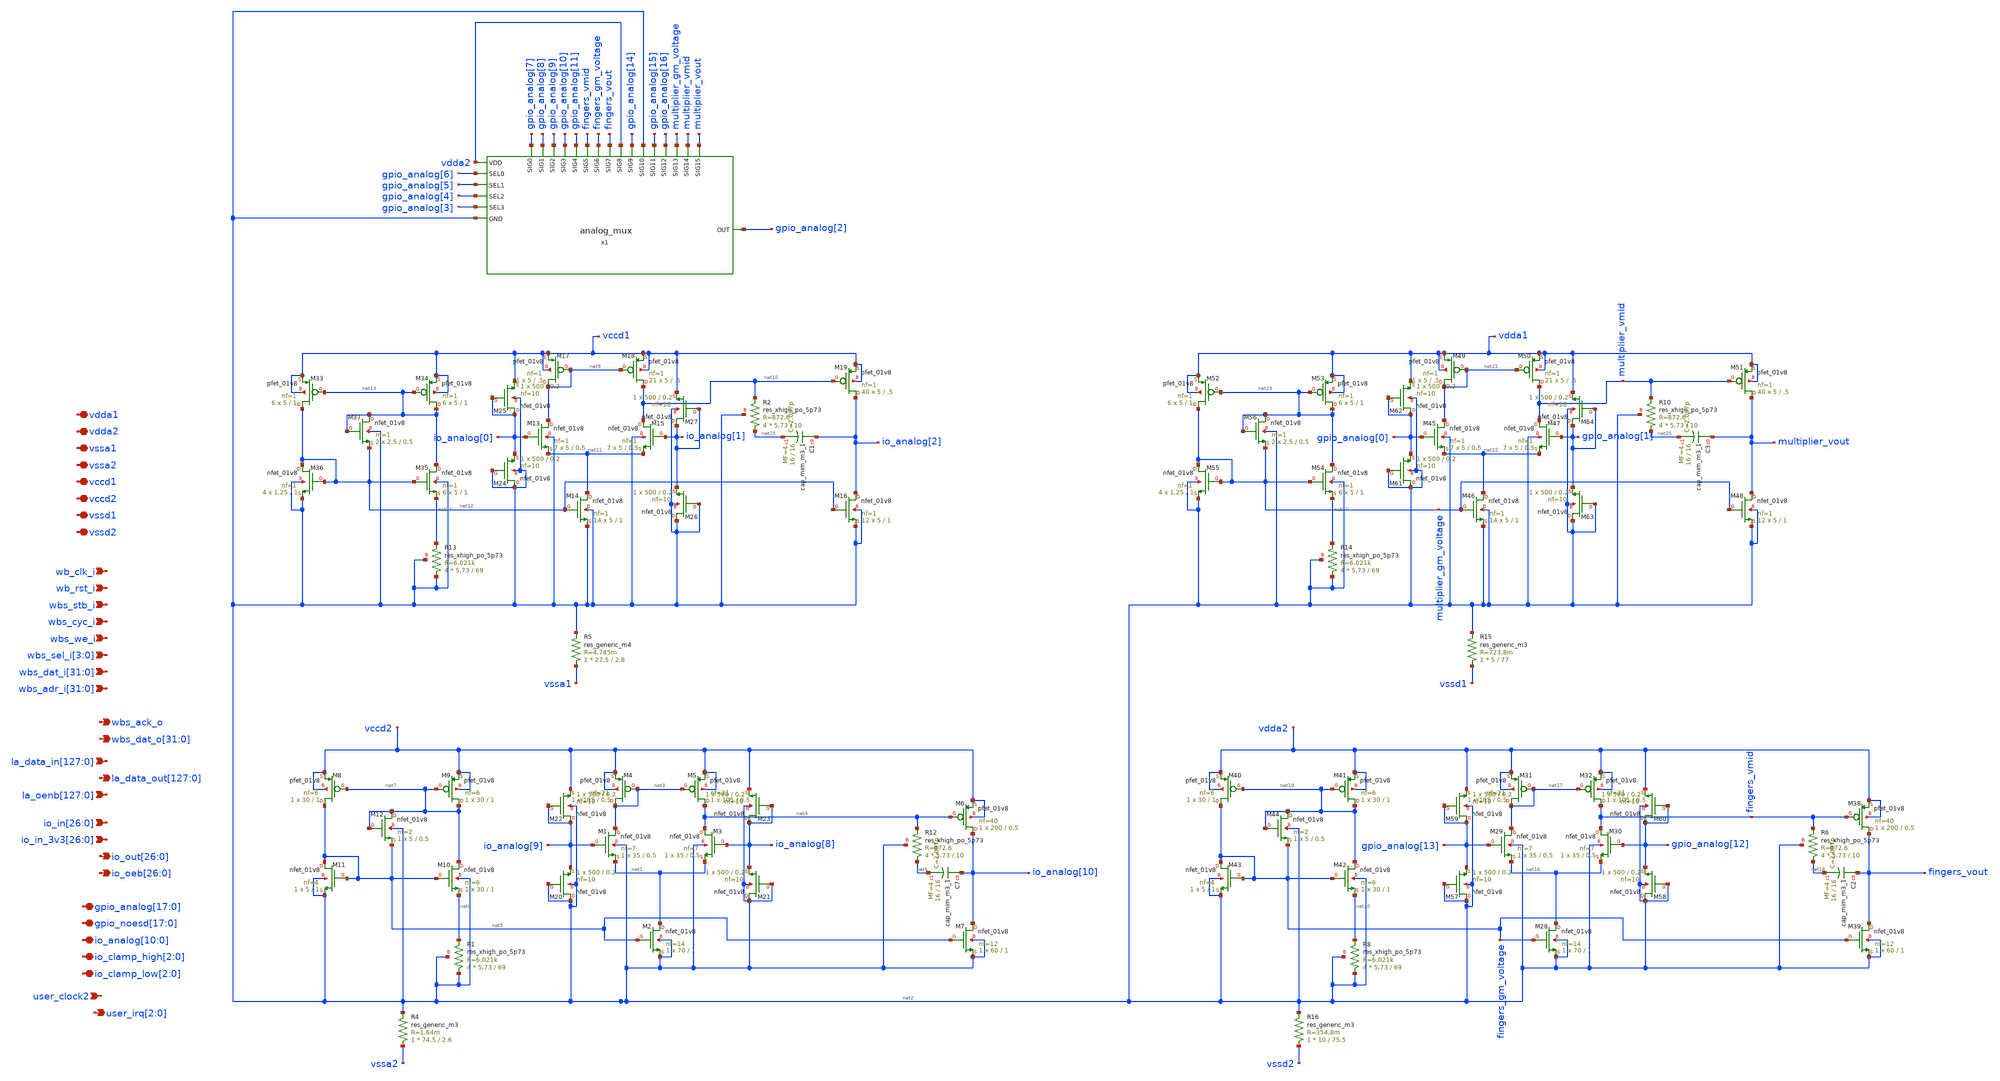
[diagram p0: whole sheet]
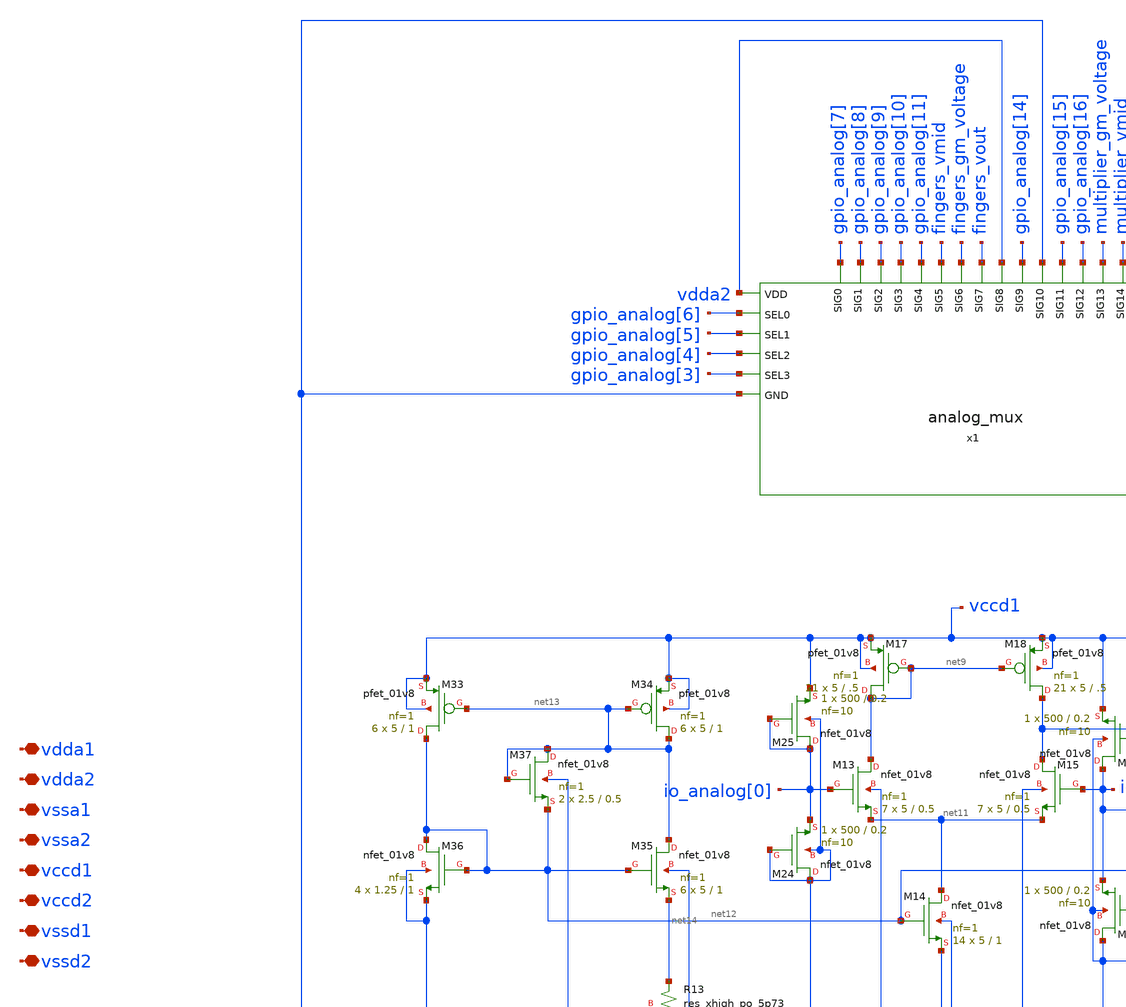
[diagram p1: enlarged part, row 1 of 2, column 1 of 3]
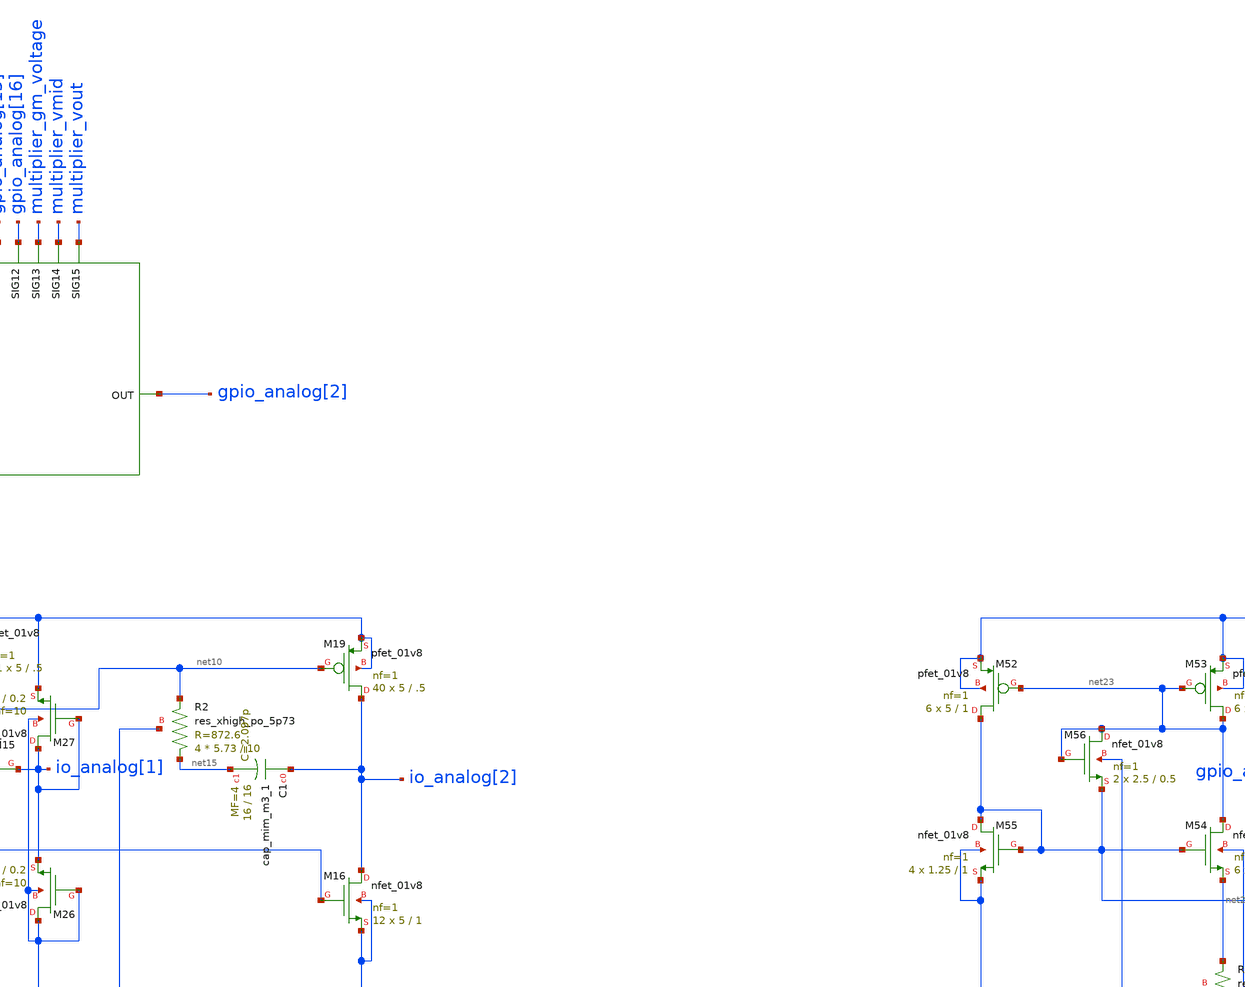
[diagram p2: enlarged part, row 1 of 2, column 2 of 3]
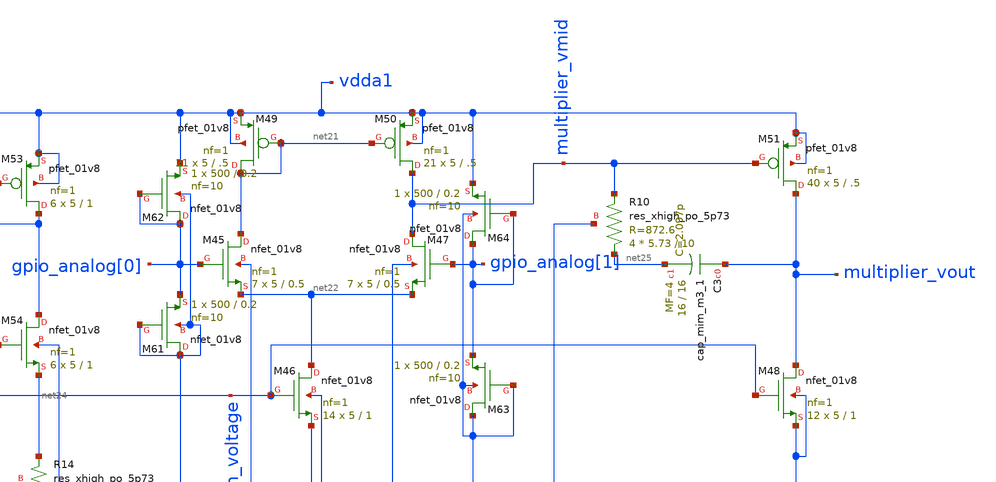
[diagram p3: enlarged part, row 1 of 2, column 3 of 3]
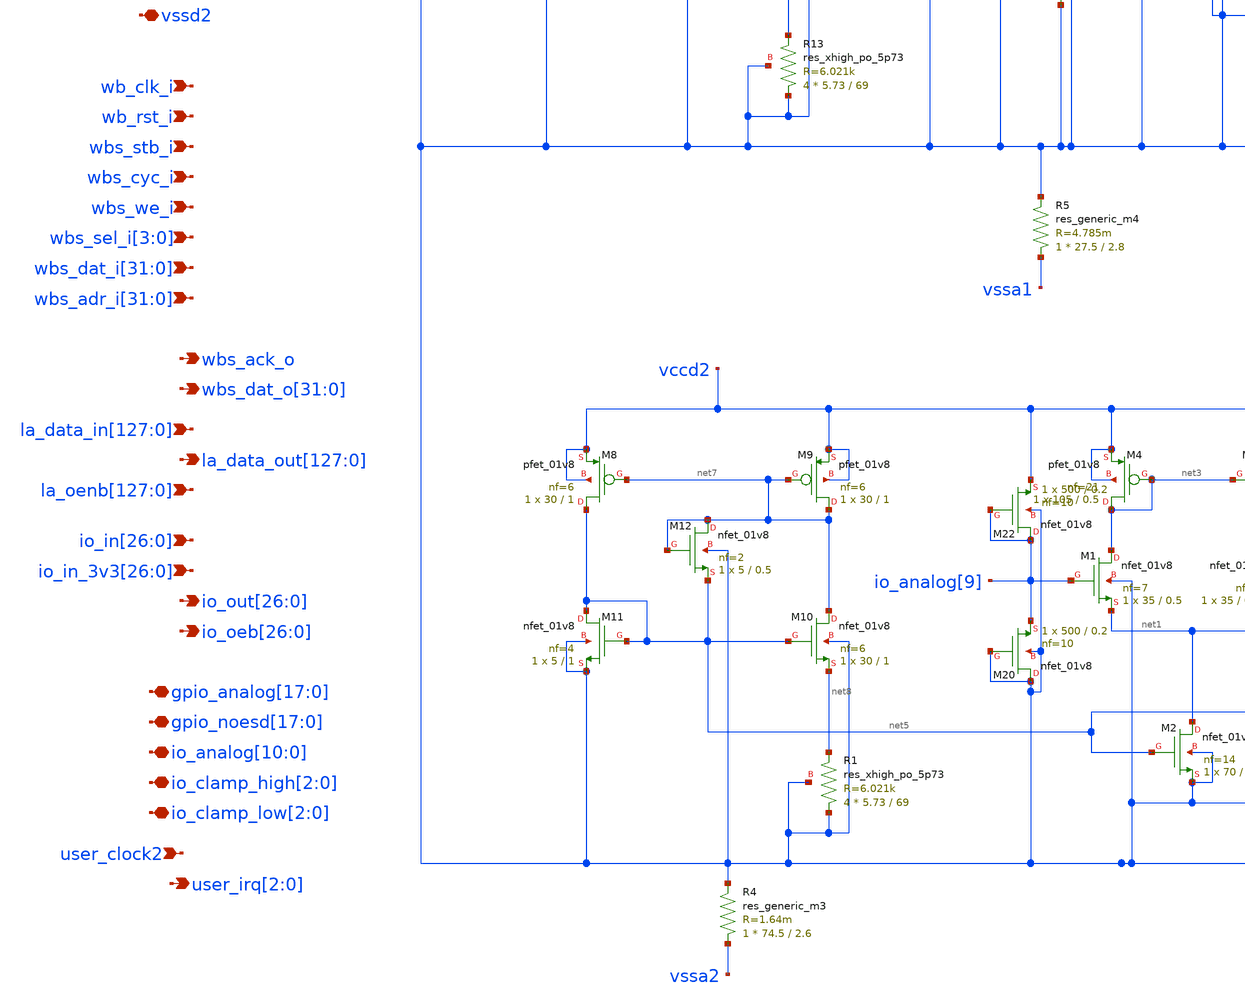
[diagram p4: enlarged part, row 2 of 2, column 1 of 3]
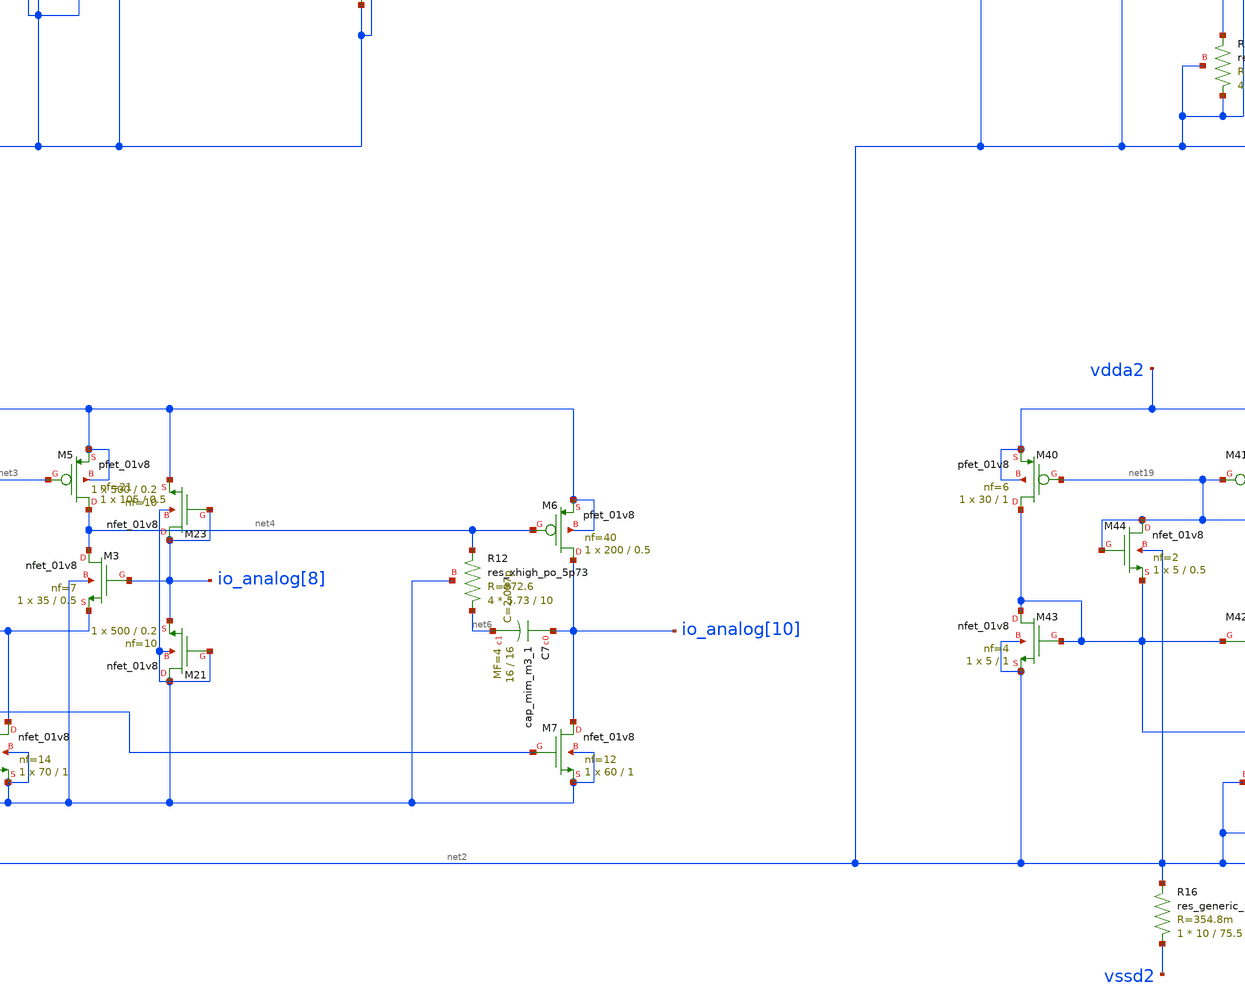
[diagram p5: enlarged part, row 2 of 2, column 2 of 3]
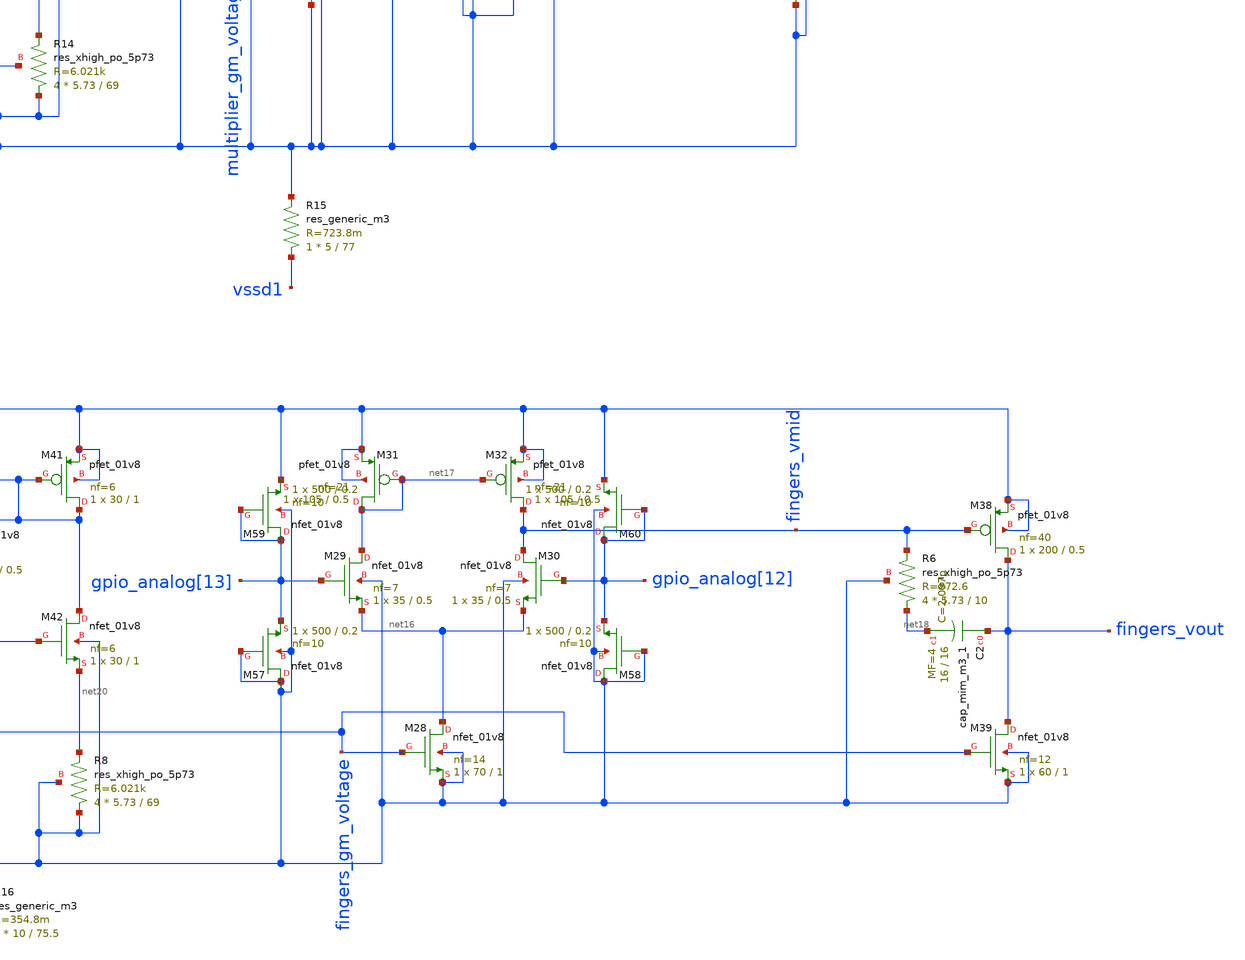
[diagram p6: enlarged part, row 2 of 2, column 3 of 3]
** sch_path: SP23_Tapeout/C2S2_Analog_TestChip-main/xschem/user_analog_project_wrapper.sch

.include $::SKYWATER_STDCELLS/sky130_fd_sc_hd.spice

**.subckt user_analog_project_wrapper vdda1 vdda2 vssa1 vssa2 vccd1 vccd2 vssd1 vssd2 wb_clk_i
*+ wb_rst_i wbs_stb_i wbs_cyc_i wbs_we_i wbs_sel_i[3],wbs_sel_i[2],wbs_sel_i[1],wbs_sel_i[0]
*+ wbs_dat_i[31],wbs_dat_i[30],wbs_dat_i[29],wbs_dat_i[28],wbs_dat_i[27],wbs_dat_i[26],wbs_dat_i[25],wbs_dat_i[24],wbs_dat_i[23],wbs_dat_i[22],wbs_dat_i[21],wbs_dat_i[20],wbs_dat_i[19],wbs_dat_i[18],wbs_dat_i[17],wbs_dat_i[16],wbs_dat_i[15],wbs_dat_i[14],wbs_dat_i[13],wbs_dat_i[12],wbs_dat_i[11],wbs_dat_i[10],wbs_dat_i[9],wbs_dat_i[8],wbs_dat_i[7],wbs_dat_i[6],wbs_dat_i[5],wbs_dat_i[4],wbs_dat_i[3],wbs_dat_i[2],wbs_dat_i[1],wbs_dat_i[0]
*+ wbs_adr_i[31],wbs_adr_i[30],wbs_adr_i[29],wbs_adr_i[28],wbs_adr_i[27],wbs_adr_i[26],wbs_adr_i[25],wbs_adr_i[24],wbs_adr_i[23],wbs_adr_i[22],wbs_adr_i[21],wbs_adr_i[20],wbs_adr_i[19],wbs_adr_i[18],wbs_adr_i[17],wbs_adr_i[16],wbs_adr_i[15],wbs_adr_i[14],wbs_adr_i[13],wbs_adr_i[12],wbs_adr_i[11],wbs_adr_i[10],wbs_adr_i[9],wbs_adr_i[8],wbs_adr_i[7],wbs_adr_i[6],wbs_adr_i[5],wbs_adr_i[4],wbs_adr_i[3],wbs_adr_i[2],wbs_adr_i[1],wbs_adr_i[0] wbs_ack_o
*+ wbs_dat_o[31],wbs_dat_o[30],wbs_dat_o[29],wbs_dat_o[28],wbs_dat_o[27],wbs_dat_o[26],wbs_dat_o[25],wbs_dat_o[24],wbs_dat_o[23],wbs_dat_o[22],wbs_dat_o[21],wbs_dat_o[20],wbs_dat_o[19],wbs_dat_o[18],wbs_dat_o[17],wbs_dat_o[16],wbs_dat_o[15],wbs_dat_o[14],wbs_dat_o[13],wbs_dat_o[12],wbs_dat_o[11],wbs_dat_o[10],wbs_dat_o[9],wbs_dat_o[8],wbs_dat_o[7],wbs_dat_o[6],wbs_dat_o[5],wbs_dat_o[4],wbs_dat_o[3],wbs_dat_o[2],wbs_dat_o[1],wbs_dat_o[0]
*+ la_data_in[127],la_data_in[126],la_data_in[125],la_data_in[124],la_data_in[123],la_data_in[122],la_data_in[121],la_data_in[120],la_data_in[119],la_data_in[118],la_data_in[117],la_data_in[116],la_data_in[115],la_data_in[114],la_data_in[113],la_data_in[112],la_data_in[111],la_data_in[110],la_data_in[109],la_data_in[108],la_data_in[107],la_data_in[106],la_data_in[105],la_data_in[104],la_data_in[103],la_data_in[102],la_data_in[101],la_data_in[100],la_data_in[99],la_data_in[98],la_data_in[97],la_data_in[96],la_data_in[95],la_data_in[94],la_data_in[93],la_data_in[92],la_data_in[91],la_data_in[90],la_data_in[89],la_data_in[88],la_data_in[87],la_data_in[86],la_data_in[85],la_data_in[84],la_data_in[83],la_data_in[82],la_data_in[81],la_data_in[80],la_data_in[79],la_data_in[78],la_data_in[77],la_data_in[76],la_data_in[75],la_data_in[74],la_data_in[73],la_data_in[72],la_data_in[71],la_data_in[70],la_data_in[69],la_data_in[68],la_data_in[67],la_data_in[66],la_data_in[65],la_data_in[64],la_data_in[63],la_data_in[62],la_data_in[61],la_data_in[60],la_data_in[59],la_data_in[58],la_data_in[57],la_data_in[56],la_data_in[55],la_data_in[54],la_data_in[53],la_data_in[52],la_data_in[51],la_data_in[50],la_data_in[49],la_data_in[48],la_data_in[47],la_data_in[46],la_data_in[45],la_data_in[44],la_data_in[43],la_data_in[42],la_data_in[41],la_data_in[40],la_data_in[39],la_data_in[38],la_data_in[37],la_data_in[36],la_data_in[35],la_data_in[34],la_data_in[33],la_data_in[32],la_data_in[31],la_data_in[30],la_data_in[29],la_data_in[28],la_data_in[27],la_data_in[26],la_data_in[25],la_data_in[24],la_data_in[23],la_data_in[22],la_data_in[21],la_data_in[20],la_data_in[19],la_data_in[18],la_data_in[17],la_data_in[16],la_data_in[15],la_data_in[14],la_data_in[13],la_data_in[12],la_data_in[11],la_data_in[10],la_data_in[9],la_data_in[8],la_data_in[7],la_data_in[6],la_data_in[5],la_data_in[4],la_data_in[3],la_data_in[2],la_data_in[1],la_data_in[0]
*+ la_data_out[127],la_data_out[126],la_data_out[125],la_data_out[124],la_data_out[123],la_data_out[122],la_data_out[121],la_data_out[120],la_data_out[119],la_data_out[118],la_data_out[117],la_data_out[116],la_data_out[115],la_data_out[114],la_data_out[113],la_data_out[112],la_data_out[111],la_data_out[110],la_data_out[109],la_data_out[108],la_data_out[107],la_data_out[106],la_data_out[105],la_data_out[104],la_data_out[103],la_data_out[102],la_data_out[101],la_data_out[100],la_data_out[99],la_data_out[98],la_data_out[97],la_data_out[96],la_data_out[95],la_data_out[94],la_data_out[93],la_data_out[92],la_data_out[91],la_data_out[90],la_data_out[89],la_data_out[88],la_data_out[87],la_data_out[86],la_data_out[85],la_data_out[84],la_data_out[83],la_data_out[82],la_data_out[81],la_data_out[80],la_data_out[79],la_data_out[78],la_data_out[77],la_data_out[76],la_data_out[75],la_data_out[74],la_data_out[73],la_data_out[72],la_data_out[71],la_data_out[70],la_data_out[69],la_data_out[68],la_data_out[67],la_data_out[66],la_data_out[65],la_data_out[64],la_data_out[63],la_data_out[62],la_data_out[61],la_data_out[60],la_data_out[59],la_data_out[58],la_data_out[57],la_data_out[56],la_data_out[55],la_data_out[54],la_data_out[53],la_data_out[52],la_data_out[51],la_data_out[50],la_data_out[49],la_data_out[48],la_data_out[47],la_data_out[46],la_data_out[45],la_data_out[44],la_data_out[43],la_data_out[42],la_data_out[41],la_data_out[40],la_data_out[39],la_data_out[38],la_data_out[37],la_data_out[36],la_data_out[35],la_data_out[34],la_data_out[33],la_data_out[32],la_data_out[31],la_data_out[30],la_data_out[29],la_data_out[28],la_data_out[27],la_data_out[26],la_data_out[25],la_data_out[24],la_data_out[23],la_data_out[22],la_data_out[21],la_data_out[20],la_data_out[19],la_data_out[18],la_data_out[17],la_data_out[16],la_data_out[15],la_data_out[14],la_data_out[13],la_data_out[12],la_data_out[11],la_data_out[10],la_data_out[9],la_data_out[8],la_data_out[7],la_data_out[6],la_data_out[5],la_data_out[4],la_data_out[3],la_data_out[2],la_data_out[1],la_data_out[0]
*+ io_in[26],io_in[25],io_in[24],io_in[23],io_in[22],io_in[21],io_in[20],io_in[19],io_in[18],io_in[17],io_in[16],io_in[15],io_in[14],io_in[13],io_in[12],io_in[11],io_in[10],io_in[9],io_in[8],io_in[7],io_in[6],io_in[5],io_in[4],io_in[3],io_in[2],io_in[1],io_in[0]
*+ io_in_3v3[26],io_in_3v3[25],io_in_3v3[24],io_in_3v3[23],io_in_3v3[22],io_in_3v3[21],io_in_3v3[20],io_in_3v3[19],io_in_3v3[18],io_in_3v3[17],io_in_3v3[16],io_in_3v3[15],io_in_3v3[14],io_in_3v3[13],io_in_3v3[12],io_in_3v3[11],io_in_3v3[10],io_in_3v3[9],io_in_3v3[8],io_in_3v3[7],io_in_3v3[6],io_in_3v3[5],io_in_3v3[4],io_in_3v3[3],io_in_3v3[2],io_in_3v3[1],io_in_3v3[0] user_clock2
*+ io_out[26],io_out[25],io_out[24],io_out[23],io_out[22],io_out[21],io_out[20],io_out[19],io_out[18],io_out[17],io_out[16],io_out[15],io_out[14],io_out[13],io_out[12],io_out[11],io_out[10],io_out[9],io_out[8],io_out[7],io_out[6],io_out[5],io_out[4],io_out[3],io_out[2],io_out[1],io_out[0]
*+ io_oeb[26],io_oeb[25],io_oeb[24],io_oeb[23],io_oeb[22],io_oeb[21],io_oeb[20],io_oeb[19],io_oeb[18],io_oeb[17],io_oeb[16],io_oeb[15],io_oeb[14],io_oeb[13],io_oeb[12],io_oeb[11],io_oeb[10],io_oeb[9],io_oeb[8],io_oeb[7],io_oeb[6],io_oeb[5],io_oeb[4],io_oeb[3],io_oeb[2],io_oeb[1],io_oeb[0]
*+ gpio_analog[17],gpio_analog[16],gpio_analog[15],gpio_analog[14],gpio_analog[13],gpio_analog[12],gpio_analog[11],gpio_analog[10],gpio_analog[9],gpio_analog[8],gpio_analog[7],gpio_analog[6],gpio_analog[5],gpio_analog[4],gpio_analog[3],gpio_analog[2],gpio_analog[1],gpio_analog[0]
*+ gpio_noesd[17],gpio_noesd[16],gpio_noesd[15],gpio_noesd[14],gpio_noesd[13],gpio_noesd[12],gpio_noesd[11],gpio_noesd[10],gpio_noesd[9],gpio_noesd[8],gpio_noesd[7],gpio_noesd[6],gpio_noesd[5],gpio_noesd[4],gpio_noesd[3],gpio_noesd[2],gpio_noesd[1],gpio_noesd[0]
*+ io_analog[10],io_analog[9],io_analog[8],io_analog[7],io_analog[6],io_analog[5],io_analog[4],io_analog[3],io_analog[2],io_analog[1],io_analog[0] io_clamp_high[2],io_clamp_high[1],io_clamp_high[0] io_clamp_low[2],io_clamp_low[1],io_clamp_low[0]
*+ user_irq[2],user_irq[1],user_irq[0]
*+ la_oenb[127],la_oenb[126],la_oenb[125],la_oenb[124],la_oenb[123],la_oenb[122],la_oenb[121],la_oenb[120],la_oenb[119],la_oenb[118],la_oenb[117],la_oenb[116],la_oenb[115],la_oenb[114],la_oenb[113],la_oenb[112],la_oenb[111],la_oenb[110],la_oenb[109],la_oenb[108],la_oenb[107],la_oenb[106],la_oenb[105],la_oenb[104],la_oenb[103],la_oenb[102],la_oenb[101],la_oenb[100],la_oenb[99],la_oenb[98],la_oenb[97],la_oenb[96],la_oenb[95],la_oenb[94],la_oenb[93],la_oenb[92],la_oenb[91],la_oenb[90],la_oenb[89],la_oenb[88],la_oenb[87],la_oenb[86],la_oenb[85],la_oenb[84],la_oenb[83],la_oenb[82],la_oenb[81],la_oenb[80],la_oenb[79],la_oenb[78],la_oenb[77],la_oenb[76],la_oenb[75],la_oenb[74],la_oenb[73],la_oenb[72],la_oenb[71],la_oenb[70],la_oenb[69],la_oenb[68],la_oenb[67],la_oenb[66],la_oenb[65],la_oenb[64],la_oenb[63],la_oenb[62],la_oenb[61],la_oenb[60],la_oenb[59],la_oenb[58],la_oenb[57],la_oenb[56],la_oenb[55],la_oenb[54],la_oenb[53],la_oenb[52],la_oenb[51],la_oenb[50],la_oenb[49],la_oenb[48],la_oenb[47],la_oenb[46],la_oenb[45],la_oenb[44],la_oenb[43],la_oenb[42],la_oenb[41],la_oenb[40],la_oenb[39],la_oenb[38],la_oenb[37],la_oenb[36],la_oenb[35],la_oenb[34],la_oenb[33],la_oenb[32],la_oenb[31],la_oenb[30],la_oenb[29],la_oenb[28],la_oenb[27],la_oenb[26],la_oenb[25],la_oenb[24],la_oenb[23],la_oenb[22],la_oenb[21],la_oenb[20],la_oenb[19],la_oenb[18],la_oenb[17],la_oenb[16],la_oenb[15],la_oenb[14],la_oenb[13],la_oenb[12],la_oenb[11],la_oenb[10],la_oenb[9],la_oenb[8],la_oenb[7],la_oenb[6],la_oenb[5],la_oenb[4],la_oenb[3],la_oenb[2],la_oenb[1],la_oenb[0]
*.iopin vdda1
*.iopin vdda2
*.iopin vssa1
*.iopin vssa2
*.iopin vccd1
*.iopin vccd2
*.iopin vssd1
*.iopin vssd2
*.ipin wb_clk_i
*.ipin wb_rst_i
*.ipin wbs_stb_i
*.ipin wbs_cyc_i
*.ipin wbs_we_i
*.ipin wbs_sel_i[3],wbs_sel_i[2],wbs_sel_i[1],wbs_sel_i[0]
*.ipin
*+ wbs_dat_i[31],wbs_dat_i[30],wbs_dat_i[29],wbs_dat_i[28],wbs_dat_i[27],wbs_dat_i[26],wbs_dat_i[25],wbs_dat_i[24],wbs_dat_i[23],wbs_dat_i[22],wbs_dat_i[21],wbs_dat_i[20],wbs_dat_i[19],wbs_dat_i[18],wbs_dat_i[17],wbs_dat_i[16],wbs_dat_i[15],wbs_dat_i[14],wbs_dat_i[13],wbs_dat_i[12],wbs_dat_i[11],wbs_dat_i[10],wbs_dat_i[9],wbs_dat_i[8],wbs_dat_i[7],wbs_dat_i[6],wbs_dat_i[5],wbs_dat_i[4],wbs_dat_i[3],wbs_dat_i[2],wbs_dat_i[1],wbs_dat_i[0]
*.ipin
*+ wbs_adr_i[31],wbs_adr_i[30],wbs_adr_i[29],wbs_adr_i[28],wbs_adr_i[27],wbs_adr_i[26],wbs_adr_i[25],wbs_adr_i[24],wbs_adr_i[23],wbs_adr_i[22],wbs_adr_i[21],wbs_adr_i[20],wbs_adr_i[19],wbs_adr_i[18],wbs_adr_i[17],wbs_adr_i[16],wbs_adr_i[15],wbs_adr_i[14],wbs_adr_i[13],wbs_adr_i[12],wbs_adr_i[11],wbs_adr_i[10],wbs_adr_i[9],wbs_adr_i[8],wbs_adr_i[7],wbs_adr_i[6],wbs_adr_i[5],wbs_adr_i[4],wbs_adr_i[3],wbs_adr_i[2],wbs_adr_i[1],wbs_adr_i[0]
*.opin wbs_ack_o
*.opin
*+ wbs_dat_o[31],wbs_dat_o[30],wbs_dat_o[29],wbs_dat_o[28],wbs_dat_o[27],wbs_dat_o[26],wbs_dat_o[25],wbs_dat_o[24],wbs_dat_o[23],wbs_dat_o[22],wbs_dat_o[21],wbs_dat_o[20],wbs_dat_o[19],wbs_dat_o[18],wbs_dat_o[17],wbs_dat_o[16],wbs_dat_o[15],wbs_dat_o[14],wbs_dat_o[13],wbs_dat_o[12],wbs_dat_o[11],wbs_dat_o[10],wbs_dat_o[9],wbs_dat_o[8],wbs_dat_o[7],wbs_dat_o[6],wbs_dat_o[5],wbs_dat_o[4],wbs_dat_o[3],wbs_dat_o[2],wbs_dat_o[1],wbs_dat_o[0]
*.ipin
*+ la_data_in[127],la_data_in[126],la_data_in[125],la_data_in[124],la_data_in[123],la_data_in[122],la_data_in[121],la_data_in[120],la_data_in[119],la_data_in[118],la_data_in[117],la_data_in[116],la_data_in[115],la_data_in[114],la_data_in[113],la_data_in[112],la_data_in[111],la_data_in[110],la_data_in[109],la_data_in[108],la_data_in[107],la_data_in[106],la_data_in[105],la_data_in[104],la_data_in[103],la_data_in[102],la_data_in[101],la_data_in[100],la_data_in[99],la_data_in[98],la_data_in[97],la_data_in[96],la_data_in[95],la_data_in[94],la_data_in[93],la_data_in[92],la_data_in[91],la_data_in[90],la_data_in[89],la_data_in[88],la_data_in[87],la_data_in[86],la_data_in[85],la_data_in[84],la_data_in[83],la_data_in[82],la_data_in[81],la_data_in[80],la_data_in[79],la_data_in[78],la_data_in[77],la_data_in[76],la_data_in[75],la_data_in[74],la_data_in[73],la_data_in[72],la_data_in[71],la_data_in[70],la_data_in[69],la_data_in[68],la_data_in[67],la_data_in[66],la_data_in[65],la_data_in[64],la_data_in[63],la_data_in[62],la_data_in[61],la_data_in[60],la_data_in[59],la_data_in[58],la_data_in[57],la_data_in[56],la_data_in[55],la_data_in[54],la_data_in[53],la_data_in[52],la_data_in[51],la_data_in[50],la_data_in[49],la_data_in[48],la_data_in[47],la_data_in[46],la_data_in[45],la_data_in[44],la_data_in[43],la_data_in[42],la_data_in[41],la_data_in[40],la_data_in[39],la_data_in[38],la_data_in[37],la_data_in[36],la_data_in[35],la_data_in[34],la_data_in[33],la_data_in[32],la_data_in[31],la_data_in[30],la_data_in[29],la_data_in[28],la_data_in[27],la_data_in[26],la_data_in[25],la_data_in[24],la_data_in[23],la_data_in[22],la_data_in[21],la_data_in[20],la_data_in[19],la_data_in[18],la_data_in[17],la_data_in[16],la_data_in[15],la_data_in[14],la_data_in[13],la_data_in[12],la_data_in[11],la_data_in[10],la_data_in[9],la_data_in[8],la_data_in[7],la_data_in[6],la_data_in[5],la_data_in[4],la_data_in[3],la_data_in[2],la_data_in[1],la_data_in[0]
*.opin
*+ la_data_out[127],la_data_out[126],la_data_out[125],la_data_out[124],la_data_out[123],la_data_out[122],la_data_out[121],la_data_out[120],la_data_out[119],la_data_out[118],la_data_out[117],la_data_out[116],la_data_out[115],la_data_out[114],la_data_out[113],la_data_out[112],la_data_out[111],la_data_out[110],la_data_out[109],la_data_out[108],la_data_out[107],la_data_out[106],la_data_out[105],la_data_out[104],la_data_out[103],la_data_out[102],la_data_out[101],la_data_out[100],la_data_out[99],la_data_out[98],la_data_out[97],la_data_out[96],la_data_out[95],la_data_out[94],la_data_out[93],la_data_out[92],la_data_out[91],la_data_out[90],la_data_out[89],la_data_out[88],la_data_out[87],la_data_out[86],la_data_out[85],la_data_out[84],la_data_out[83],la_data_out[82],la_data_out[81],la_data_out[80],la_data_out[79],la_data_out[78],la_data_out[77],la_data_out[76],la_data_out[75],la_data_out[74],la_data_out[73],la_data_out[72],la_data_out[71],la_data_out[70],la_data_out[69],la_data_out[68],la_data_out[67],la_data_out[66],la_data_out[65],la_data_out[64],la_data_out[63],la_data_out[62],la_data_out[61],la_data_out[60],la_data_out[59],la_data_out[58],la_data_out[57],la_data_out[56],la_data_out[55],la_data_out[54],la_data_out[53],la_data_out[52],la_data_out[51],la_data_out[50],la_data_out[49],la_data_out[48],la_data_out[47],la_data_out[46],la_data_out[45],la_data_out[44],la_data_out[43],la_data_out[42],la_data_out[41],la_data_out[40],la_data_out[39],la_data_out[38],la_data_out[37],la_data_out[36],la_data_out[35],la_data_out[34],la_data_out[33],la_data_out[32],la_data_out[31],la_data_out[30],la_data_out[29],la_data_out[28],la_data_out[27],la_data_out[26],la_data_out[25],la_data_out[24],la_data_out[23],la_data_out[22],la_data_out[21],la_data_out[20],la_data_out[19],la_data_out[18],la_data_out[17],la_data_out[16],la_data_out[15],la_data_out[14],la_data_out[13],la_data_out[12],la_data_out[11],la_data_out[10],la_data_out[9],la_data_out[8],la_data_out[7],la_data_out[6],la_data_out[5],la_data_out[4],la_data_out[3],la_data_out[2],la_data_out[1],la_data_out[0]
*.ipin
*+ io_in[26],io_in[25],io_in[24],io_in[23],io_in[22],io_in[21],io_in[20],io_in[19],io_in[18],io_in[17],io_in[16],io_in[15],io_in[14],io_in[13],io_in[12],io_in[11],io_in[10],io_in[9],io_in[8],io_in[7],io_in[6],io_in[5],io_in[4],io_in[3],io_in[2],io_in[1],io_in[0]
*.ipin
*+ io_in_3v3[26],io_in_3v3[25],io_in_3v3[24],io_in_3v3[23],io_in_3v3[22],io_in_3v3[21],io_in_3v3[20],io_in_3v3[19],io_in_3v3[18],io_in_3v3[17],io_in_3v3[16],io_in_3v3[15],io_in_3v3[14],io_in_3v3[13],io_in_3v3[12],io_in_3v3[11],io_in_3v3[10],io_in_3v3[9],io_in_3v3[8],io_in_3v3[7],io_in_3v3[6],io_in_3v3[5],io_in_3v3[4],io_in_3v3[3],io_in_3v3[2],io_in_3v3[1],io_in_3v3[0]
*.ipin user_clock2
*.opin
*+ io_out[26],io_out[25],io_out[24],io_out[23],io_out[22],io_out[21],io_out[20],io_out[19],io_out[18],io_out[17],io_out[16],io_out[15],io_out[14],io_out[13],io_out[12],io_out[11],io_out[10],io_out[9],io_out[8],io_out[7],io_out[6],io_out[5],io_out[4],io_out[3],io_out[2],io_out[1],io_out[0]
*.opin
*+ io_oeb[26],io_oeb[25],io_oeb[24],io_oeb[23],io_oeb[22],io_oeb[21],io_oeb[20],io_oeb[19],io_oeb[18],io_oeb[17],io_oeb[16],io_oeb[15],io_oeb[14],io_oeb[13],io_oeb[12],io_oeb[11],io_oeb[10],io_oeb[9],io_oeb[8],io_oeb[7],io_oeb[6],io_oeb[5],io_oeb[4],io_oeb[3],io_oeb[2],io_oeb[1],io_oeb[0]
*.iopin
*+ gpio_analog[17],gpio_analog[16],gpio_analog[15],gpio_analog[14],gpio_analog[13],gpio_analog[12],gpio_analog[11],gpio_analog[10],gpio_analog[9],gpio_analog[8],gpio_analog[7],gpio_analog[6],gpio_analog[5],gpio_analog[4],gpio_analog[3],gpio_analog[2],gpio_analog[1],gpio_analog[0]
*.iopin
*+ gpio_noesd[17],gpio_noesd[16],gpio_noesd[15],gpio_noesd[14],gpio_noesd[13],gpio_noesd[12],gpio_noesd[11],gpio_noesd[10],gpio_noesd[9],gpio_noesd[8],gpio_noesd[7],gpio_noesd[6],gpio_noesd[5],gpio_noesd[4],gpio_noesd[3],gpio_noesd[2],gpio_noesd[1],gpio_noesd[0]
*.iopin
*+ io_analog[10],io_analog[9],io_analog[8],io_analog[7],io_analog[6],io_analog[5],io_analog[4],io_analog[3],io_analog[2],io_analog[1],io_analog[0]
*.iopin io_clamp_high[2],io_clamp_high[1],io_clamp_high[0]
*.iopin io_clamp_low[2],io_clamp_low[1],io_clamp_low[0]
*.opin user_irq[2],user_irq[1],user_irq[0]
*.ipin
*+ la_oenb[127],la_oenb[126],la_oenb[125],la_oenb[124],la_oenb[123],la_oenb[122],la_oenb[121],la_oenb[120],la_oenb[119],la_oenb[118],la_oenb[117],la_oenb[116],la_oenb[115],la_oenb[114],la_oenb[113],la_oenb[112],la_oenb[111],la_oenb[110],la_oenb[109],la_oenb[108],la_oenb[107],la_oenb[106],la_oenb[105],la_oenb[104],la_oenb[103],la_oenb[102],la_oenb[101],la_oenb[100],la_oenb[99],la_oenb[98],la_oenb[97],la_oenb[96],la_oenb[95],la_oenb[94],la_oenb[93],la_oenb[92],la_oenb[91],la_oenb[90],la_oenb[89],la_oenb[88],la_oenb[87],la_oenb[86],la_oenb[85],la_oenb[84],la_oenb[83],la_oenb[82],la_oenb[81],la_oenb[80],la_oenb[79],la_oenb[78],la_oenb[77],la_oenb[76],la_oenb[75],la_oenb[74],la_oenb[73],la_oenb[72],la_oenb[71],la_oenb[70],la_oenb[69],la_oenb[68],la_oenb[67],la_oenb[66],la_oenb[65],la_oenb[64],la_oenb[63],la_oenb[62],la_oenb[61],la_oenb[60],la_oenb[59],la_oenb[58],la_oenb[57],la_oenb[56],la_oenb[55],la_oenb[54],la_oenb[53],la_oenb[52],la_oenb[51],la_oenb[50],la_oenb[49],la_oenb[48],la_oenb[47],la_oenb[46],la_oenb[45],la_oenb[44],la_oenb[43],la_oenb[42],la_oenb[41],la_oenb[40],la_oenb[39],la_oenb[38],la_oenb[37],la_oenb[36],la_oenb[35],la_oenb[34],la_oenb[33],la_oenb[32],la_oenb[31],la_oenb[30],la_oenb[29],la_oenb[28],la_oenb[27],la_oenb[26],la_oenb[25],la_oenb[24],la_oenb[23],la_oenb[22],la_oenb[21],la_oenb[20],la_oenb[19],la_oenb[18],la_oenb[17],la_oenb[16],la_oenb[15],la_oenb[14],la_oenb[13],la_oenb[12],la_oenb[11],la_oenb[10],la_oenb[9],la_oenb[8],la_oenb[7],la_oenb[6],la_oenb[5],la_oenb[4],la_oenb[3],la_oenb[2],la_oenb[1],la_oenb[0]
XM2 net1 net5 net2 net2 sky130_fd_pr__nfet_01v8 L=1 W=70 nf=14 ad='int((nf+1)/2) * W/nf * 0.29' as='int((nf+2)/2) * W/nf * 0.29'
+ pd='2*int((nf+1)/2) * (W/nf + 0.29)' ps='2*int((nf+2)/2) * (W/nf + 0.29)' nrd='0.29 / W' nrs='0.29 / W'
+ sa=0 sb=0 sd=0 mult=1 m=1
XM1 net3 io_analog[9] net1 net2 sky130_fd_pr__nfet_01v8 L=0.5 W=35 nf=7 ad='int((nf+1)/2) * W/nf * 0.29'
+ as='int((nf+2)/2) * W/nf * 0.29' pd='2*int((nf+1)/2) * (W/nf + 0.29)' ps='2*int((nf+2)/2) * (W/nf + 0.29)'
+ nrd='0.29 / W' nrs='0.29 / W' sa=0 sb=0 sd=0 mult=1 m=1
XM3 net4 io_analog[8] net1 net2 sky130_fd_pr__nfet_01v8 L=0.5 W=35 nf=7 ad='int((nf+1)/2) * W/nf * 0.29'
+ as='int((nf+2)/2) * W/nf * 0.29' pd='2*int((nf+1)/2) * (W/nf + 0.29)' ps='2*int((nf+2)/2) * (W/nf + 0.29)'
+ nrd='0.29 / W' nrs='0.29 / W' sa=0 sb=0 sd=0 mult=1 m=1
XM4 net3 net3 vccd2 vccd2 sky130_fd_pr__pfet_01v8 L=0.5 W=105 nf=21 ad='int((nf+1)/2) * W/nf * 0.29'
+ as='int((nf+2)/2) * W/nf * 0.29' pd='2*int((nf+1)/2) * (W/nf + 0.29)' ps='2*int((nf+2)/2) * (W/nf + 0.29)'
+ nrd='0.29 / W' nrs='0.29 / W' sa=0 sb=0 sd=0 mult=1 m=1
XM5 net4 net3 vccd2 vccd2 sky130_fd_pr__pfet_01v8 L=0.5 W=105 nf=21 ad='int((nf+1)/2) * W/nf * 0.29'
+ as='int((nf+2)/2) * W/nf * 0.29' pd='2*int((nf+1)/2) * (W/nf + 0.29)' ps='2*int((nf+2)/2) * (W/nf + 0.29)'
+ nrd='0.29 / W' nrs='0.29 / W' sa=0 sb=0 sd=0 mult=1 m=1
XM6 io_analog[10] net4 vccd2 vccd2 sky130_fd_pr__pfet_01v8 L=0.5 W=200 nf=40 ad='int((nf+1)/2) * W/nf * 0.29'
+ as='int((nf+2)/2) * W/nf * 0.29' pd='2*int((nf+1)/2) * (W/nf + 0.29)' ps='2*int((nf+2)/2) * (W/nf + 0.29)'
+ nrd='0.29 / W' nrs='0.29 / W' sa=0 sb=0 sd=0 mult=1 m=1
XM7 io_analog[10] net5 net2 net2 sky130_fd_pr__nfet_01v8 L=1 W=60 nf=12 ad='int((nf+1)/2) * W/nf * 0.29'
+ as='int((nf+2)/2) * W/nf * 0.29' pd='2*int((nf+1)/2) * (W/nf + 0.29)' ps='2*int((nf+2)/2) * (W/nf + 0.29)'
+ nrd='0.29 / W' nrs='0.29 / W' sa=0 sb=0 sd=0 mult=1 m=1
XC7 io_analog[10] net6 sky130_fd_pr__cap_mim_m3_1 W=16 L=16 MF=4 m=4
XR12 net6 net4 net2 sky130_fd_pr__res_xhigh_po_5p73 L=10 mult=4 m=4
XM8 net5 net7 vccd2 vccd2 sky130_fd_pr__pfet_01v8 L=1 W=30 nf=6 ad='int((nf+1)/2) * W/nf * 0.29' as='int((nf+2)/2) * W/nf * 0.29'
+ pd='2*int((nf+1)/2) * (W/nf + 0.29)' ps='2*int((nf+2)/2) * (W/nf + 0.29)' nrd='0.29 / W' nrs='0.29 / W'
+ sa=0 sb=0 sd=0 mult=1 m=1
XM9 net7 net7 vccd2 vccd2 sky130_fd_pr__pfet_01v8 L=1 W=30 nf=6 ad='int((nf+1)/2) * W/nf * 0.29' as='int((nf+2)/2) * W/nf * 0.29'
+ pd='2*int((nf+1)/2) * (W/nf + 0.29)' ps='2*int((nf+2)/2) * (W/nf + 0.29)' nrd='0.29 / W' nrs='0.29 / W'
+ sa=0 sb=0 sd=0 mult=1 m=1
XM10 net7 net5 net8 net2 sky130_fd_pr__nfet_01v8 L=1 W=30 nf=6 ad='int((nf+1)/2) * W/nf * 0.29' as='int((nf+2)/2) * W/nf * 0.29'
+ pd='2*int((nf+1)/2) * (W/nf + 0.29)' ps='2*int((nf+2)/2) * (W/nf + 0.29)' nrd='0.29 / W' nrs='0.29 / W'
+ sa=0 sb=0 sd=0 mult=1 m=1
XM11 net5 net5 net2 net2 sky130_fd_pr__nfet_01v8 L=1 W=5 nf=4 ad='int((nf+1)/2) * W/nf * 0.29' as='int((nf+2)/2) * W/nf * 0.29'
+ pd='2*int((nf+1)/2) * (W/nf + 0.29)' ps='2*int((nf+2)/2) * (W/nf + 0.29)' nrd='0.29 / W' nrs='0.29 / W'
+ sa=0 sb=0 sd=0 mult=1 m=1
XM12 net7 net7 net5 net2 sky130_fd_pr__nfet_01v8 L=0.5 W=5 nf=2 ad='int((nf+1)/2) * W/nf * 0.29' as='int((nf+2)/2) * W/nf * 0.29'
+ pd='2*int((nf+1)/2) * (W/nf + 0.29)' ps='2*int((nf+2)/2) * (W/nf + 0.29)' nrd='0.29 / W' nrs='0.29 / W'
+ sa=0 sb=0 sd=0 mult=1 m=1
XR1 net2 net8 net2 sky130_fd_pr__res_xhigh_po_5p73 L=69 mult=4 m=4
XM13 net9 io_analog[0] net11 net2 sky130_fd_pr__nfet_01v8 L=0.5 W=5 nf=1 ad='int((nf+1)/2) * W/nf * 0.29'
+ as='int((nf+2)/2) * W/nf * 0.29' pd='2*int((nf+1)/2) * (W/nf + 0.29)' ps='2*int((nf+2)/2) * (W/nf + 0.29)'
+ nrd='0.29 / W' nrs='0.29 / W' sa=0 sb=0 sd=0 mult=7 m=7
XM14 net11 net12 net2 net2 sky130_fd_pr__nfet_01v8 L=1 W=5 nf=1 ad='int((nf+1)/2) * W/nf * 0.29' as='int((nf+2)/2) * W/nf * 0.29'
+ pd='2*int((nf+1)/2) * (W/nf + 0.29)' ps='2*int((nf+2)/2) * (W/nf + 0.29)' nrd='0.29 / W' nrs='0.29 / W'
+ sa=0 sb=0 sd=0 mult=14 m=14
XM15 net10 io_analog[1] net11 net2 sky130_fd_pr__nfet_01v8 L=0.5 W=5 nf=1 ad='int((nf+1)/2) * W/nf * 0.29'
+ as='int((nf+2)/2) * W/nf * 0.29' pd='2*int((nf+1)/2) * (W/nf + 0.29)' ps='2*int((nf+2)/2) * (W/nf + 0.29)'
+ nrd='0.29 / W' nrs='0.29 / W' sa=0 sb=0 sd=0 mult=7 m=7
XM16 io_analog[2] net12 net2 net2 sky130_fd_pr__nfet_01v8 L=1 W=5 nf=1 ad='int((nf+1)/2) * W/nf * 0.29'
+ as='int((nf+2)/2) * W/nf * 0.29' pd='2*int((nf+1)/2) * (W/nf + 0.29)' ps='2*int((nf+2)/2) * (W/nf + 0.29)'
+ nrd='0.29 / W' nrs='0.29 / W' sa=0 sb=0 sd=0 mult=12 m=12
XM17 net9 net9 vccd1 vccd1 sky130_fd_pr__pfet_01v8 L=.5 W=5 nf=1 ad='int((nf+1)/2) * W/nf * 0.29' as='int((nf+2)/2) * W/nf * 0.29'
+ pd='2*int((nf+1)/2) * (W/nf + 0.29)' ps='2*int((nf+2)/2) * (W/nf + 0.29)' nrd='0.29 / W' nrs='0.29 / W'
+ sa=0 sb=0 sd=0 mult=21 m=21
XM18 net10 net9 vccd1 vccd1 sky130_fd_pr__pfet_01v8 L=.5 W=5 nf=1 ad='int((nf+1)/2) * W/nf * 0.29' as='int((nf+2)/2) * W/nf * 0.29'
+ pd='2*int((nf+1)/2) * (W/nf + 0.29)' ps='2*int((nf+2)/2) * (W/nf + 0.29)' nrd='0.29 / W' nrs='0.29 / W'
+ sa=0 sb=0 sd=0 mult=21 m=21
XM19 io_analog[2] net10 vccd1 vccd1 sky130_fd_pr__pfet_01v8 L=.5 W=5 nf=1 ad='int((nf+1)/2) * W/nf * 0.29'
+ as='int((nf+2)/2) * W/nf * 0.29' pd='2*int((nf+1)/2) * (W/nf + 0.29)' ps='2*int((nf+2)/2) * (W/nf + 0.29)'
+ nrd='0.29 / W' nrs='0.29 / W' sa=0 sb=0 sd=0 mult=40 m=40
XR2 net15 net10 net2 sky130_fd_pr__res_xhigh_po_5p73 L=10 mult=4 m=4
XC1 io_analog[2] net15 sky130_fd_pr__cap_mim_m3_1 W=16 L=16 MF=4 m=4
XM33 net12 net13 vccd1 vccd1 sky130_fd_pr__pfet_01v8 L=1 W=5 nf=1 ad='int((nf+1)/2) * W/nf * 0.29' as='int((nf+2)/2) * W/nf * 0.29'
+ pd='2*int((nf+1)/2) * (W/nf + 0.29)' ps='2*int((nf+2)/2) * (W/nf + 0.29)' nrd='0.29 / W' nrs='0.29 / W'
+ sa=0 sb=0 sd=0 mult=6 m=6
XM34 net13 net13 vccd1 vccd1 sky130_fd_pr__pfet_01v8 L=1 W=5 nf=1 ad='int((nf+1)/2) * W/nf * 0.29' as='int((nf+2)/2) * W/nf * 0.29'
+ pd='2*int((nf+1)/2) * (W/nf + 0.29)' ps='2*int((nf+2)/2) * (W/nf + 0.29)' nrd='0.29 / W' nrs='0.29 / W'
+ sa=0 sb=0 sd=0 mult=6 m=6
XM35 net13 net12 net14 net2 sky130_fd_pr__nfet_01v8 L=1 W=5 nf=1 ad='int((nf+1)/2) * W/nf * 0.29' as='int((nf+2)/2) * W/nf * 0.29'
+ pd='2*int((nf+1)/2) * (W/nf + 0.29)' ps='2*int((nf+2)/2) * (W/nf + 0.29)' nrd='0.29 / W' nrs='0.29 / W'
+ sa=0 sb=0 sd=0 mult=6 m=6
XM36 net12 net12 net2 net2 sky130_fd_pr__nfet_01v8 L=1 W=1.25 nf=1 ad='int((nf+1)/2) * W/nf * 0.29' as='int((nf+2)/2) * W/nf * 0.29'
+ pd='2*int((nf+1)/2) * (W/nf + 0.29)' ps='2*int((nf+2)/2) * (W/nf + 0.29)' nrd='0.29 / W' nrs='0.29 / W'
+ sa=0 sb=0 sd=0 mult=4 m=4
XM37 net13 net13 net12 net2 sky130_fd_pr__nfet_01v8 L=0.5 W=2.5 nf=1 ad='int((nf+1)/2) * W/nf * 0.29'
+ as='int((nf+2)/2) * W/nf * 0.29' pd='2*int((nf+1)/2) * (W/nf + 0.29)' ps='2*int((nf+2)/2) * (W/nf + 0.29)'
+ nrd='0.29 / W' nrs='0.29 / W' sa=0 sb=0 sd=0 mult=2 m=2
XR13 net2 net14 net2 sky130_fd_pr__res_xhigh_po_5p73 L=69 mult=4 m=4
R5 vssa1 net2 sky130_fd_pr__res_generic_m4 W=27.5 L=2.8 m=1
R4 vssa2 net2 sky130_fd_pr__res_generic_m3 W=74.5 L=2.6 m=1
XM20 net2 net2 io_analog[9] net2 sky130_fd_pr__nfet_01v8 L=0.2 W=500 nf=10 ad='int((nf+1)/2) * W/nf * 0.29'
+ as='int((nf+2)/2) * W/nf * 0.29' pd='2*int((nf+1)/2) * (W/nf + 0.29)' ps='2*int((nf+2)/2) * (W/nf + 0.29)'
+ nrd='0.29 / W' nrs='0.29 / W' sa=0 sb=0 sd=0 mult=1 m=1
XM21 net2 net2 io_analog[8] net2 sky130_fd_pr__nfet_01v8 L=0.2 W=500 nf=10 ad='int((nf+1)/2) * W/nf * 0.29'
+ as='int((nf+2)/2) * W/nf * 0.29' pd='2*int((nf+1)/2) * (W/nf + 0.29)' ps='2*int((nf+2)/2) * (W/nf + 0.29)'
+ nrd='0.29 / W' nrs='0.29 / W' sa=0 sb=0 sd=0 mult=1 m=1
XM22 io_analog[9] io_analog[9] vccd2 net2 sky130_fd_pr__nfet_01v8 L=0.2 W=500 nf=10 ad='int((nf+1)/2) * W/nf * 0.29'
+ as='int((nf+2)/2) * W/nf * 0.29' pd='2*int((nf+1)/2) * (W/nf + 0.29)' ps='2*int((nf+2)/2) * (W/nf + 0.29)'
+ nrd='0.29 / W' nrs='0.29 / W' sa=0 sb=0 sd=0 mult=1 m=1
XM23 io_analog[8] io_analog[8] vccd2 net2 sky130_fd_pr__nfet_01v8 L=0.2 W=500 nf=10 ad='int((nf+1)/2) * W/nf * 0.29'
+ as='int((nf+2)/2) * W/nf * 0.29' pd='2*int((nf+1)/2) * (W/nf + 0.29)' ps='2*int((nf+2)/2) * (W/nf + 0.29)'
+ nrd='0.29 / W' nrs='0.29 / W' sa=0 sb=0 sd=0 mult=1 m=1
XM24 net2 net2 io_analog[0] net2 sky130_fd_pr__nfet_01v8 L=0.2 W=500 nf=10 ad='int((nf+1)/2) * W/nf * 0.29'
+ as='int((nf+2)/2) * W/nf * 0.29' pd='2*int((nf+1)/2) * (W/nf + 0.29)' ps='2*int((nf+2)/2) * (W/nf + 0.29)'
+ nrd='0.29 / W' nrs='0.29 / W' sa=0 sb=0 sd=0 mult=1 m=1
XM25 io_analog[0] io_analog[0] vccd1 net2 sky130_fd_pr__nfet_01v8 L=0.2 W=500 nf=10 ad='int((nf+1)/2) * W/nf * 0.29'
+ as='int((nf+2)/2) * W/nf * 0.29' pd='2*int((nf+1)/2) * (W/nf + 0.29)' ps='2*int((nf+2)/2) * (W/nf + 0.29)'
+ nrd='0.29 / W' nrs='0.29 / W' sa=0 sb=0 sd=0 mult=1 m=1
XM26 net2 net2 io_analog[1] net2 sky130_fd_pr__nfet_01v8 L=0.2 W=500 nf=10 ad='int((nf+1)/2) * W/nf * 0.29'
+ as='int((nf+2)/2) * W/nf * 0.29' pd='2*int((nf+1)/2) * (W/nf + 0.29)' ps='2*int((nf+2)/2) * (W/nf + 0.29)'
+ nrd='0.29 / W' nrs='0.29 / W' sa=0 sb=0 sd=0 mult=1 m=1
XM27 io_analog[1] io_analog[1] vccd1 net2 sky130_fd_pr__nfet_01v8 L=0.2 W=500 nf=10 ad='int((nf+1)/2) * W/nf * 0.29'
+ as='int((nf+2)/2) * W/nf * 0.29' pd='2*int((nf+1)/2) * (W/nf + 0.29)' ps='2*int((nf+2)/2) * (W/nf + 0.29)'
+ nrd='0.29 / W' nrs='0.29 / W' sa=0 sb=0 sd=0 mult=1 m=1
x1 multiplier_vout multiplier_vmid multiplier_gm_voltage gpio_analog[16] gpio_analog[15] net2
+ gpio_analog[14] vdda2 fingers_vout fingers_gm_voltage fingers_vmid gpio_analog[11] gpio_analog[10] gpio_analog[9]
+ gpio_analog[8] gpio_analog[7] vdda2 net2 gpio_analog[6] gpio_analog[5] gpio_analog[4] gpio_analog[3]
+ gpio_analog[2] analog_mux
XM28 net16 fingers_gm_voltage net2 net2 sky130_fd_pr__nfet_01v8 L=1 W=70 nf=14 ad='int((nf+1)/2) * W/nf * 0.29'
+ as='int((nf+2)/2) * W/nf * 0.29' pd='2*int((nf+1)/2) * (W/nf + 0.29)' ps='2*int((nf+2)/2) * (W/nf + 0.29)'
+ nrd='0.29 / W' nrs='0.29 / W' sa=0 sb=0 sd=0 mult=1 m=1
XM29 net17 gpio_analog[13] net16 net2 sky130_fd_pr__nfet_01v8 L=0.5 W=35 nf=7 ad='int((nf+1)/2) * W/nf * 0.29'
+ as='int((nf+2)/2) * W/nf * 0.29' pd='2*int((nf+1)/2) * (W/nf + 0.29)' ps='2*int((nf+2)/2) * (W/nf + 0.29)'
+ nrd='0.29 / W' nrs='0.29 / W' sa=0 sb=0 sd=0 mult=1 m=1
XM30 fingers_vmid gpio_analog[12] net16 net2 sky130_fd_pr__nfet_01v8 L=0.5 W=35 nf=7 ad='int((nf+1)/2) * W/nf * 0.29'
+ as='int((nf+2)/2) * W/nf * 0.29' pd='2*int((nf+1)/2) * (W/nf + 0.29)' ps='2*int((nf+2)/2) * (W/nf + 0.29)'
+ nrd='0.29 / W' nrs='0.29 / W' sa=0 sb=0 sd=0 mult=1 m=1
XM31 net17 net17 vdda2 vdda2 sky130_fd_pr__pfet_01v8 L=0.5 W=105 nf=21 ad='int((nf+1)/2) * W/nf * 0.29'
+ as='int((nf+2)/2) * W/nf * 0.29' pd='2*int((nf+1)/2) * (W/nf + 0.29)' ps='2*int((nf+2)/2) * (W/nf + 0.29)'
+ nrd='0.29 / W' nrs='0.29 / W' sa=0 sb=0 sd=0 mult=1 m=1
XM32 fingers_vmid net17 vdda2 vdda2 sky130_fd_pr__pfet_01v8 L=0.5 W=105 nf=21 ad='int((nf+1)/2) * W/nf * 0.29'
+ as='int((nf+2)/2) * W/nf * 0.29' pd='2*int((nf+1)/2) * (W/nf + 0.29)' ps='2*int((nf+2)/2) * (W/nf + 0.29)'
+ nrd='0.29 / W' nrs='0.29 / W' sa=0 sb=0 sd=0 mult=1 m=1
XM38 fingers_vout fingers_vmid vdda2 vdda2 sky130_fd_pr__pfet_01v8 L=0.5 W=200 nf=40 ad='int((nf+1)/2) * W/nf * 0.29'
+ as='int((nf+2)/2) * W/nf * 0.29' pd='2*int((nf+1)/2) * (W/nf + 0.29)' ps='2*int((nf+2)/2) * (W/nf + 0.29)'
+ nrd='0.29 / W' nrs='0.29 / W' sa=0 sb=0 sd=0 mult=1 m=1
XM39 fingers_vout fingers_gm_voltage net2 net2 sky130_fd_pr__nfet_01v8 L=1 W=60 nf=12 ad='int((nf+1)/2) * W/nf * 0.29'
+ as='int((nf+2)/2) * W/nf * 0.29' pd='2*int((nf+1)/2) * (W/nf + 0.29)' ps='2*int((nf+2)/2) * (W/nf + 0.29)'
+ nrd='0.29 / W' nrs='0.29 / W' sa=0 sb=0 sd=0 mult=1 m=1
XC2 fingers_vout net18 sky130_fd_pr__cap_mim_m3_1 W=16 L=16 MF=4 m=4
XR6 net18 fingers_vmid net2 sky130_fd_pr__res_xhigh_po_5p73 L=10 mult=4 m=4
XM40 fingers_gm_voltage net19 vdda2 vdda2 sky130_fd_pr__pfet_01v8 L=1 W=30 nf=6 ad='int((nf+1)/2) * W/nf * 0.29'
+ as='int((nf+2)/2) * W/nf * 0.29' pd='2*int((nf+1)/2) * (W/nf + 0.29)' ps='2*int((nf+2)/2) * (W/nf + 0.29)'
+ nrd='0.29 / W' nrs='0.29 / W' sa=0 sb=0 sd=0 mult=1 m=1
XM41 net19 net19 vdda2 vdda2 sky130_fd_pr__pfet_01v8 L=1 W=30 nf=6 ad='int((nf+1)/2) * W/nf * 0.29' as='int((nf+2)/2) * W/nf * 0.29'
+ pd='2*int((nf+1)/2) * (W/nf + 0.29)' ps='2*int((nf+2)/2) * (W/nf + 0.29)' nrd='0.29 / W' nrs='0.29 / W'
+ sa=0 sb=0 sd=0 mult=1 m=1
XM42 net19 fingers_gm_voltage net20 net2 sky130_fd_pr__nfet_01v8 L=1 W=30 nf=6 ad='int((nf+1)/2) * W/nf * 0.29'
+ as='int((nf+2)/2) * W/nf * 0.29' pd='2*int((nf+1)/2) * (W/nf + 0.29)' ps='2*int((nf+2)/2) * (W/nf + 0.29)'
+ nrd='0.29 / W' nrs='0.29 / W' sa=0 sb=0 sd=0 mult=1 m=1
XM43 fingers_gm_voltage fingers_gm_voltage net2 net2 sky130_fd_pr__nfet_01v8 L=1 W=5 nf=4 ad='int((nf+1)/2) * W/nf * 0.29'
+ as='int((nf+2)/2) * W/nf * 0.29' pd='2*int((nf+1)/2) * (W/nf + 0.29)' ps='2*int((nf+2)/2) * (W/nf + 0.29)'
+ nrd='0.29 / W' nrs='0.29 / W' sa=0 sb=0 sd=0 mult=1 m=1
XM44 net19 net19 fingers_gm_voltage net2 sky130_fd_pr__nfet_01v8 L=0.5 W=5 nf=2 ad='int((nf+1)/2) * W/nf * 0.29'
+ as='int((nf+2)/2) * W/nf * 0.29' pd='2*int((nf+1)/2) * (W/nf + 0.29)' ps='2*int((nf+2)/2) * (W/nf + 0.29)'
+ nrd='0.29 / W' nrs='0.29 / W' sa=0 sb=0 sd=0 mult=1 m=1
XR8 net2 net20 net2 sky130_fd_pr__res_xhigh_po_5p73 L=69 mult=4 m=4
XM45 net21 gpio_analog[0] net22 net2 sky130_fd_pr__nfet_01v8 L=0.5 W=5 nf=1 ad='int((nf+1)/2) * W/nf * 0.29'
+ as='int((nf+2)/2) * W/nf * 0.29' pd='2*int((nf+1)/2) * (W/nf + 0.29)' ps='2*int((nf+2)/2) * (W/nf + 0.29)'
+ nrd='0.29 / W' nrs='0.29 / W' sa=0 sb=0 sd=0 mult=7 m=7
XM46 net22 multiplier_gm_voltage net2 net2 sky130_fd_pr__nfet_01v8 L=1 W=5 nf=1 ad='int((nf+1)/2) * W/nf * 0.29'
+ as='int((nf+2)/2) * W/nf * 0.29' pd='2*int((nf+1)/2) * (W/nf + 0.29)' ps='2*int((nf+2)/2) * (W/nf + 0.29)'
+ nrd='0.29 / W' nrs='0.29 / W' sa=0 sb=0 sd=0 mult=14 m=14
XM47 multiplier_vmid gpio_analog[1] net22 net2 sky130_fd_pr__nfet_01v8 L=0.5 W=5 nf=1 ad='int((nf+1)/2) * W/nf * 0.29'
+ as='int((nf+2)/2) * W/nf * 0.29' pd='2*int((nf+1)/2) * (W/nf + 0.29)' ps='2*int((nf+2)/2) * (W/nf + 0.29)'
+ nrd='0.29 / W' nrs='0.29 / W' sa=0 sb=0 sd=0 mult=7 m=7
XM48 multiplier_vout multiplier_gm_voltage net2 net2 sky130_fd_pr__nfet_01v8 L=1 W=5 nf=1 ad='int((nf+1)/2) * W/nf * 0.29'
+ as='int((nf+2)/2) * W/nf * 0.29' pd='2*int((nf+1)/2) * (W/nf + 0.29)' ps='2*int((nf+2)/2) * (W/nf + 0.29)'
+ nrd='0.29 / W' nrs='0.29 / W' sa=0 sb=0 sd=0 mult=12 m=12
XM49 net21 net21 vdda1 vdda1 sky130_fd_pr__pfet_01v8 L=.5 W=5 nf=1 ad='int((nf+1)/2) * W/nf * 0.29' as='int((nf+2)/2) * W/nf * 0.29'
+ pd='2*int((nf+1)/2) * (W/nf + 0.29)' ps='2*int((nf+2)/2) * (W/nf + 0.29)' nrd='0.29 / W' nrs='0.29 / W'
+ sa=0 sb=0 sd=0 mult=21 m=21
XM50 multiplier_vmid net21 vdda1 vdda1 sky130_fd_pr__pfet_01v8 L=.5 W=5 nf=1 ad='int((nf+1)/2) * W/nf * 0.29'
+ as='int((nf+2)/2) * W/nf * 0.29' pd='2*int((nf+1)/2) * (W/nf + 0.29)' ps='2*int((nf+2)/2) * (W/nf + 0.29)'
+ nrd='0.29 / W' nrs='0.29 / W' sa=0 sb=0 sd=0 mult=21 m=21
XM51 multiplier_vout multiplier_vmid vdda1 vdda1 sky130_fd_pr__pfet_01v8 L=.5 W=5 nf=1 ad='int((nf+1)/2) * W/nf * 0.29'
+ as='int((nf+2)/2) * W/nf * 0.29' pd='2*int((nf+1)/2) * (W/nf + 0.29)' ps='2*int((nf+2)/2) * (W/nf + 0.29)'
+ nrd='0.29 / W' nrs='0.29 / W' sa=0 sb=0 sd=0 mult=40 m=40
XR10 net25 multiplier_vmid net2 sky130_fd_pr__res_xhigh_po_5p73 L=10 mult=4 m=4
XC3 multiplier_vout net25 sky130_fd_pr__cap_mim_m3_1 W=16 L=16 MF=4 m=4
XM52 multiplier_gm_voltage net23 vdda1 vdda1 sky130_fd_pr__pfet_01v8 L=1 W=5 nf=1 ad='int((nf+1)/2) * W/nf * 0.29'
+ as='int((nf+2)/2) * W/nf * 0.29' pd='2*int((nf+1)/2) * (W/nf + 0.29)' ps='2*int((nf+2)/2) * (W/nf + 0.29)'
+ nrd='0.29 / W' nrs='0.29 / W' sa=0 sb=0 sd=0 mult=6 m=6
XM53 net23 net23 vdda1 vdda1 sky130_fd_pr__pfet_01v8 L=1 W=5 nf=1 ad='int((nf+1)/2) * W/nf * 0.29' as='int((nf+2)/2) * W/nf * 0.29'
+ pd='2*int((nf+1)/2) * (W/nf + 0.29)' ps='2*int((nf+2)/2) * (W/nf + 0.29)' nrd='0.29 / W' nrs='0.29 / W'
+ sa=0 sb=0 sd=0 mult=6 m=6
XM54 net23 multiplier_gm_voltage net24 net2 sky130_fd_pr__nfet_01v8 L=1 W=5 nf=1 ad='int((nf+1)/2) * W/nf * 0.29'
+ as='int((nf+2)/2) * W/nf * 0.29' pd='2*int((nf+1)/2) * (W/nf + 0.29)' ps='2*int((nf+2)/2) * (W/nf + 0.29)'
+ nrd='0.29 / W' nrs='0.29 / W' sa=0 sb=0 sd=0 mult=6 m=6
XM55 multiplier_gm_voltage multiplier_gm_voltage net2 net2 sky130_fd_pr__nfet_01v8 L=1 W=1.25 nf=1 ad='int((nf+1)/2) * W/nf * 0.29'
+ as='int((nf+2)/2) * W/nf * 0.29' pd='2*int((nf+1)/2) * (W/nf + 0.29)' ps='2*int((nf+2)/2) * (W/nf + 0.29)'
+ nrd='0.29 / W' nrs='0.29 / W' sa=0 sb=0 sd=0 mult=4 m=4
XM56 net23 net23 multiplier_gm_voltage net2 sky130_fd_pr__nfet_01v8 L=0.5 W=2.5 nf=1 ad='int((nf+1)/2) * W/nf * 0.29'
+ as='int((nf+2)/2) * W/nf * 0.29' pd='2*int((nf+1)/2) * (W/nf + 0.29)' ps='2*int((nf+2)/2) * (W/nf + 0.29)'
+ nrd='0.29 / W' nrs='0.29 / W' sa=0 sb=0 sd=0 mult=2 m=2
XR14 net2 net24 net2 sky130_fd_pr__res_xhigh_po_5p73 L=69 mult=4 m=4
R15 vssd1 net2 sky130_fd_pr__res_generic_m3 W=5 L=77 m=1
R16 vssd2 net2 sky130_fd_pr__res_generic_m3 W=10 L=75.5 m=1
XM57 net2 net2 gpio_analog[13] net2 sky130_fd_pr__nfet_01v8 L=0.2 W=500 nf=10 ad='int((nf+1)/2) * W/nf * 0.29'
+ as='int((nf+2)/2) * W/nf * 0.29' pd='2*int((nf+1)/2) * (W/nf + 0.29)' ps='2*int((nf+2)/2) * (W/nf + 0.29)'
+ nrd='0.29 / W' nrs='0.29 / W' sa=0 sb=0 sd=0 mult=1 m=1
XM58 net2 net2 gpio_analog[12] net2 sky130_fd_pr__nfet_01v8 L=0.2 W=500 nf=10 ad='int((nf+1)/2) * W/nf * 0.29'
+ as='int((nf+2)/2) * W/nf * 0.29' pd='2*int((nf+1)/2) * (W/nf + 0.29)' ps='2*int((nf+2)/2) * (W/nf + 0.29)'
+ nrd='0.29 / W' nrs='0.29 / W' sa=0 sb=0 sd=0 mult=1 m=1
XM59 gpio_analog[13] gpio_analog[13] vdda2 net2 sky130_fd_pr__nfet_01v8 L=0.2 W=500 nf=10 ad='int((nf+1)/2) * W/nf * 0.29'
+ as='int((nf+2)/2) * W/nf * 0.29' pd='2*int((nf+1)/2) * (W/nf + 0.29)' ps='2*int((nf+2)/2) * (W/nf + 0.29)'
+ nrd='0.29 / W' nrs='0.29 / W' sa=0 sb=0 sd=0 mult=1 m=1
XM60 gpio_analog[12] gpio_analog[12] vdda2 net2 sky130_fd_pr__nfet_01v8 L=0.2 W=500 nf=10 ad='int((nf+1)/2) * W/nf * 0.29'
+ as='int((nf+2)/2) * W/nf * 0.29' pd='2*int((nf+1)/2) * (W/nf + 0.29)' ps='2*int((nf+2)/2) * (W/nf + 0.29)'
+ nrd='0.29 / W' nrs='0.29 / W' sa=0 sb=0 sd=0 mult=1 m=1
XM61 net2 net2 gpio_analog[0] net2 sky130_fd_pr__nfet_01v8 L=0.2 W=500 nf=10 ad='int((nf+1)/2) * W/nf * 0.29'
+ as='int((nf+2)/2) * W/nf * 0.29' pd='2*int((nf+1)/2) * (W/nf + 0.29)' ps='2*int((nf+2)/2) * (W/nf + 0.29)'
+ nrd='0.29 / W' nrs='0.29 / W' sa=0 sb=0 sd=0 mult=1 m=1
XM62 gpio_analog[0] gpio_analog[0] vdda1 net2 sky130_fd_pr__nfet_01v8 L=0.2 W=500 nf=10 ad='int((nf+1)/2) * W/nf * 0.29'
+ as='int((nf+2)/2) * W/nf * 0.29' pd='2*int((nf+1)/2) * (W/nf + 0.29)' ps='2*int((nf+2)/2) * (W/nf + 0.29)'
+ nrd='0.29 / W' nrs='0.29 / W' sa=0 sb=0 sd=0 mult=1 m=1
XM63 net2 net2 gpio_analog[1] net2 sky130_fd_pr__nfet_01v8 L=0.2 W=500 nf=10 ad='int((nf+1)/2) * W/nf * 0.29'
+ as='int((nf+2)/2) * W/nf * 0.29' pd='2*int((nf+1)/2) * (W/nf + 0.29)' ps='2*int((nf+2)/2) * (W/nf + 0.29)'
+ nrd='0.29 / W' nrs='0.29 / W' sa=0 sb=0 sd=0 mult=1 m=1
XM64 gpio_analog[1] gpio_analog[1] vdda1 net2 sky130_fd_pr__nfet_01v8 L=0.2 W=500 nf=10 ad='int((nf+1)/2) * W/nf * 0.29'
+ as='int((nf+2)/2) * W/nf * 0.29' pd='2*int((nf+1)/2) * (W/nf + 0.29)' ps='2*int((nf+2)/2) * (W/nf + 0.29)'
+ nrd='0.29 / W' nrs='0.29 / W' sa=0 sb=0 sd=0 mult=1 m=1
**.ends

* expanding   symbol:  analog_mux.sym # of pins=23
** sym_path: SP23_Tapeout/C2S2_Analog_TestChip-main/xschem/analog_mux.sym
** sch_path: SP23_Tapeout/C2S2_Analog_TestChip-main/xschem/analog_mux.sch
.subckt analog_mux SIG15 SIG14 SIG13 SIG12 SIG11 SIG10 SIG9 SIG8 SIG7 SIG6 SIG5 SIG4 SIG3 SIG2 SIG1
+ SIG0 VDD GND SEL0 SEL1 SEL2 SEL3 OUT
*.opin OUT
*.ipin VDD
*.ipin GND
*.ipin SEL0
*.ipin SEL1
*.ipin SEL2
*.ipin SEL3
*.ipin SIG3
*.ipin SIG2
*.ipin SIG1
*.ipin SIG0
*.ipin SIG7
*.ipin SIG6
*.ipin SIG5
*.ipin SIG4
*.ipin SIG11
*.ipin SIG10
*.ipin SIG9
*.ipin SIG8
*.ipin SIG15
*.ipin SIG14
*.ipin SIG13
*.ipin SIG12
x1 VDD GND SEL0 SEL1 SEL2 SEL3 net1 net2 net4 net3 net5 net6 net8 net7 net9 net10 net12 net11 net13
+ net14 net16 net15 net17 net18 net20 net19 net21 net22 net24 net23 net25 net26 net28 net27 net29 net30
+ net32 net31 decoder_x4
x2 SIG15 net1 net2 SIG14 net4 net3 SIG13 net5 net6 SIG12 net8 net7 SIG11 net9 net10 SIG10 net12
+ net11 SIG9 net13 net14 SIG8 net16 net15 OUT SIG7 net17 net18 SIG6 net20 net19 SIG5 net21 net22 SIG4 net24
+ net23 SIG3 net25 net26 SIG2 net28 net27 SIG1 net29 net30 SIG0 net32 net31 VDD GND switch_x16
.ends


* expanding   symbol:  decoder_x4.sym # of pins=38
** sym_path: SP23_Tapeout/C2S2_Analog_TestChip-main/xschem/decoder_x4.sym
** sch_path: SP23_Tapeout/C2S2_Analog_TestChip-main/xschem/decoder_x4.sch
.subckt decoder_x4 VPWR VGND S0 S1 S2 S3 Q15N Q15 Q14N Q14 Q13N Q13 Q12N Q12 Q11N Q11 Q10N Q10 Q9N
+ Q9 Q8N Q8 Q7N Q7 Q6N Q6 Q5N Q5 Q4N Q4 Q3N Q3 Q2N Q2 Q1N Q1 Q0N Q0
*.ipin S3
*.ipin S2
*.ipin S1
*.ipin S0
*.ipin VGND
*.ipin VPWR
*.opin Q14N
*.opin Q15N
*.opin Q13N
*.opin Q12N
*.opin Q10N
*.opin Q11N
*.opin Q9N
*.opin Q8N
*.opin Q7N
*.opin Q6N
*.opin Q4N
*.opin Q3N
*.opin Q2N
*.opin Q1N
*.opin Q0N
*.opin Q5N
*.opin Q14
*.opin Q15
*.opin Q13
*.opin Q12
*.opin Q10
*.opin Q11
*.opin Q9
*.opin Q8
*.opin Q7
*.opin Q6
*.opin Q4
*.opin Q3
*.opin Q2
*.opin Q1
*.opin Q0
*.opin Q5
x17 S3 VGND VGND VPWR VPWR S3N sky130_fd_sc_hd__inv_8
x18 S2 VGND VGND VPWR VPWR S2N sky130_fd_sc_hd__inv_8
x19 S1 VGND VGND VPWR VPWR S1N sky130_fd_sc_hd__inv_8
x20 S0 VGND VGND VPWR VPWR S0N sky130_fd_sc_hd__inv_8
x21 Q0N VGND VGND VPWR VPWR Q0 sky130_fd_sc_hd__inv_2
x22 Q1N VGND VGND VPWR VPWR Q1 sky130_fd_sc_hd__inv_2
x23 Q2N VGND VGND VPWR VPWR Q2 sky130_fd_sc_hd__inv_2
x24 Q3N VGND VGND VPWR VPWR Q3 sky130_fd_sc_hd__inv_2
x1 S3N S2N S1N S0N VGND VGND VPWR VPWR Q0N sky130_fd_sc_hd__nand4_2
x2 S3N S2N S1N S0 VGND VGND VPWR VPWR Q1N sky130_fd_sc_hd__nand4_2
x3 S3N S2N S1 S0N VGND VGND VPWR VPWR Q2N sky130_fd_sc_hd__nand4_2
x4 S3N S2N S1 S0 VGND VGND VPWR VPWR Q3N sky130_fd_sc_hd__nand4_2
x5 S3N S2 S1N S0N VGND VGND VPWR VPWR Q4N sky130_fd_sc_hd__nand4_2
x6 S3N S2 S1N S0 VGND VGND VPWR VPWR Q5N sky130_fd_sc_hd__nand4_2
x7 S3N S2 S1 S0N VGND VGND VPWR VPWR Q6N sky130_fd_sc_hd__nand4_2
x8 S3N S2 S1 S0 VGND VGND VPWR VPWR Q7N sky130_fd_sc_hd__nand4_2
x9 S3 S2N S1N S0N VGND VGND VPWR VPWR Q8N sky130_fd_sc_hd__nand4_2
x10 S3 S2N S1N S0 VGND VGND VPWR VPWR Q9N sky130_fd_sc_hd__nand4_2
x11 S3 S2N S1 S0N VGND VGND VPWR VPWR Q10N sky130_fd_sc_hd__nand4_2
x12 S3 S2N S1 S0 VGND VGND VPWR VPWR Q11N sky130_fd_sc_hd__nand4_2
x13 S3 S2 S1N S0N VGND VGND VPWR VPWR Q12N sky130_fd_sc_hd__nand4_2
x14 S3 S2 S1N S0 VGND VGND VPWR VPWR Q13N sky130_fd_sc_hd__nand4_2
x15 S3 S2 S1 S0N VGND VGND VPWR VPWR Q14N sky130_fd_sc_hd__nand4_2
x16 S3 S2 S1 S0 VGND VGND VPWR VPWR Q15N sky130_fd_sc_hd__nand4_2
x25 Q4N VGND VGND VPWR VPWR Q4 sky130_fd_sc_hd__inv_2
x26 Q5N VGND VGND VPWR VPWR Q5 sky130_fd_sc_hd__inv_2
x27 Q6N VGND VGND VPWR VPWR Q6 sky130_fd_sc_hd__inv_2
x28 Q7N VGND VGND VPWR VPWR Q7 sky130_fd_sc_hd__inv_2
x29 Q8N VGND VGND VPWR VPWR Q8 sky130_fd_sc_hd__inv_2
x30 Q9N VGND VGND VPWR VPWR Q9 sky130_fd_sc_hd__inv_2
x31 Q10N VGND VGND VPWR VPWR Q10 sky130_fd_sc_hd__inv_2
x32 Q11N VGND VGND VPWR VPWR Q11 sky130_fd_sc_hd__inv_2
x33 Q12N VGND VGND VPWR VPWR Q12 sky130_fd_sc_hd__inv_2
x34 Q13N VGND VGND VPWR VPWR Q13 sky130_fd_sc_hd__inv_2
x35 Q14N VGND VGND VPWR VPWR Q14 sky130_fd_sc_hd__inv_2
x36 Q15N VGND VGND VPWR VPWR Q15 sky130_fd_sc_hd__inv_2
.ends


* expanding   symbol:  switch_x16.sym # of pins=51
** sym_path: switch_x16.sym
** sch_path: switch_x16.sch
.subckt switch_x16 S15 PG15 NG15 S14 PG14 NG14 S13 PG13 NG13 S12 PG12 NG12 S11 PG11 NG11 S10 PG10
+ NG10 S9 PG9 NG9 S8 PG8 NG8 D S7 PG7 NG7 S6 PG6 NG6 S5 PG5 NG5 S4 PG4 NG4 S3 PG3 NG3 S2 PG2 NG2 S1 PG1
+ NG1 S0 PG0 NG0 VPB VNB
*.ipin PG0
*.ipin NG0
*.ipin S0
*.ipin PG1
*.ipin NG1
*.ipin S1
*.ipin PG2
*.ipin NG2
*.ipin S2
*.ipin PG3
*.ipin NG3
*.ipin S3
*.ipin PG4
*.ipin NG4
*.ipin S4
*.ipin PG5
*.ipin NG5
*.ipin S5
*.ipin PG6
*.ipin NG6
*.ipin S6
*.ipin PG7
*.ipin NG7
*.ipin S7
*.ipin PG8
*.ipin NG8
*.ipin S8
*.ipin PG9
*.ipin NG9
*.ipin S9
*.ipin PG10
*.ipin NG10
*.ipin S10
*.ipin PG11
*.ipin NG11
*.ipin S11
*.ipin PG12
*.ipin NG12
*.ipin S12
*.ipin PG13
*.ipin NG13
*.ipin S13
*.ipin PG14
*.ipin NG14
*.ipin S14
*.ipin PG15
*.ipin NG15
*.ipin S15
*.opin D
*.ipin VPB
*.ipin VNB
x1 S0 VNB NG0 VPB PG0 D a_mux_switch
x2 S1 VNB NG1 VPB PG1 D a_mux_switch
x3 S2 VNB NG2 VPB PG2 D a_mux_switch
x4 S3 VNB NG3 VPB PG3 D a_mux_switch
x5 S4 VNB NG4 VPB PG4 D a_mux_switch
x6 S5 VNB NG5 VPB PG5 D a_mux_switch
x7 S6 VNB NG6 VPB PG6 D a_mux_switch
x8 S7 VNB NG7 VPB PG7 D a_mux_switch
x9 S8 VNB NG8 VPB PG8 D a_mux_switch
x10 S9 VNB NG9 VPB PG9 D a_mux_switch
x11 S10 VNB NG10 VPB PG10 D a_mux_switch
x15 S11 VNB NG11 VPB PG11 D a_mux_switch
x16 S12 VNB NG12 VPB PG12 D a_mux_switch
x17 S13 VNB NG13 VPB PG13 D a_mux_switch
x18 S14 VNB NG14 VPB PG14 D a_mux_switch
x19 S15 VNB NG15 VPB PG15 D a_mux_switch
.ends


* expanding   symbol:  a_mux_switch.sym # of pins=6
** sym_path: SP23_Tapeout/C2S2_Analog_TestChip-main/xschem/a_mux_switch.sym
** sch_path: SP23_Tapeout/C2S2_Analog_TestChip-main/xschem/a_mux_switch.sch
.subckt a_mux_switch VD VNB VNG VPB VPG VS
*.ipin VPG
*.ipin VNG
*.ipin VD
*.opin VS
*.ipin VPB
*.ipin VNB
XM1 VD VPG VS VPB sky130_fd_pr__pfet_01v8 L=0.15 W=95 nf=19 ad='int((nf+1)/2) * W/nf * 0.29' as='int((nf+2)/2) * W/nf * 0.29'
+ pd='2*int((nf+1)/2) * (W/nf + 0.29)' ps='2*int((nf+2)/2) * (W/nf + 0.29)' nrd='0.29 / W' nrs='0.29 / W'
+ sa=0 sb=0 sd=0 mult=1 m=1
XM2 VD VNG VS VNB sky130_fd_pr__nfet_01v8 L=0.15 W=45 nf=9 ad='int((nf+1)/2) * W/nf * 0.29' as='int((nf+2)/2) * W/nf * 0.29'
+ pd='2*int((nf+1)/2) * (W/nf + 0.29)' ps='2*int((nf+2)/2) * (W/nf + 0.29)' nrd='0.29 / W' nrs='0.29 / W'
+ sa=0 sb=0 sd=0 mult=1 m=1
.ends

.GLOBAL VPB
.GLOBAL VNB
.end
